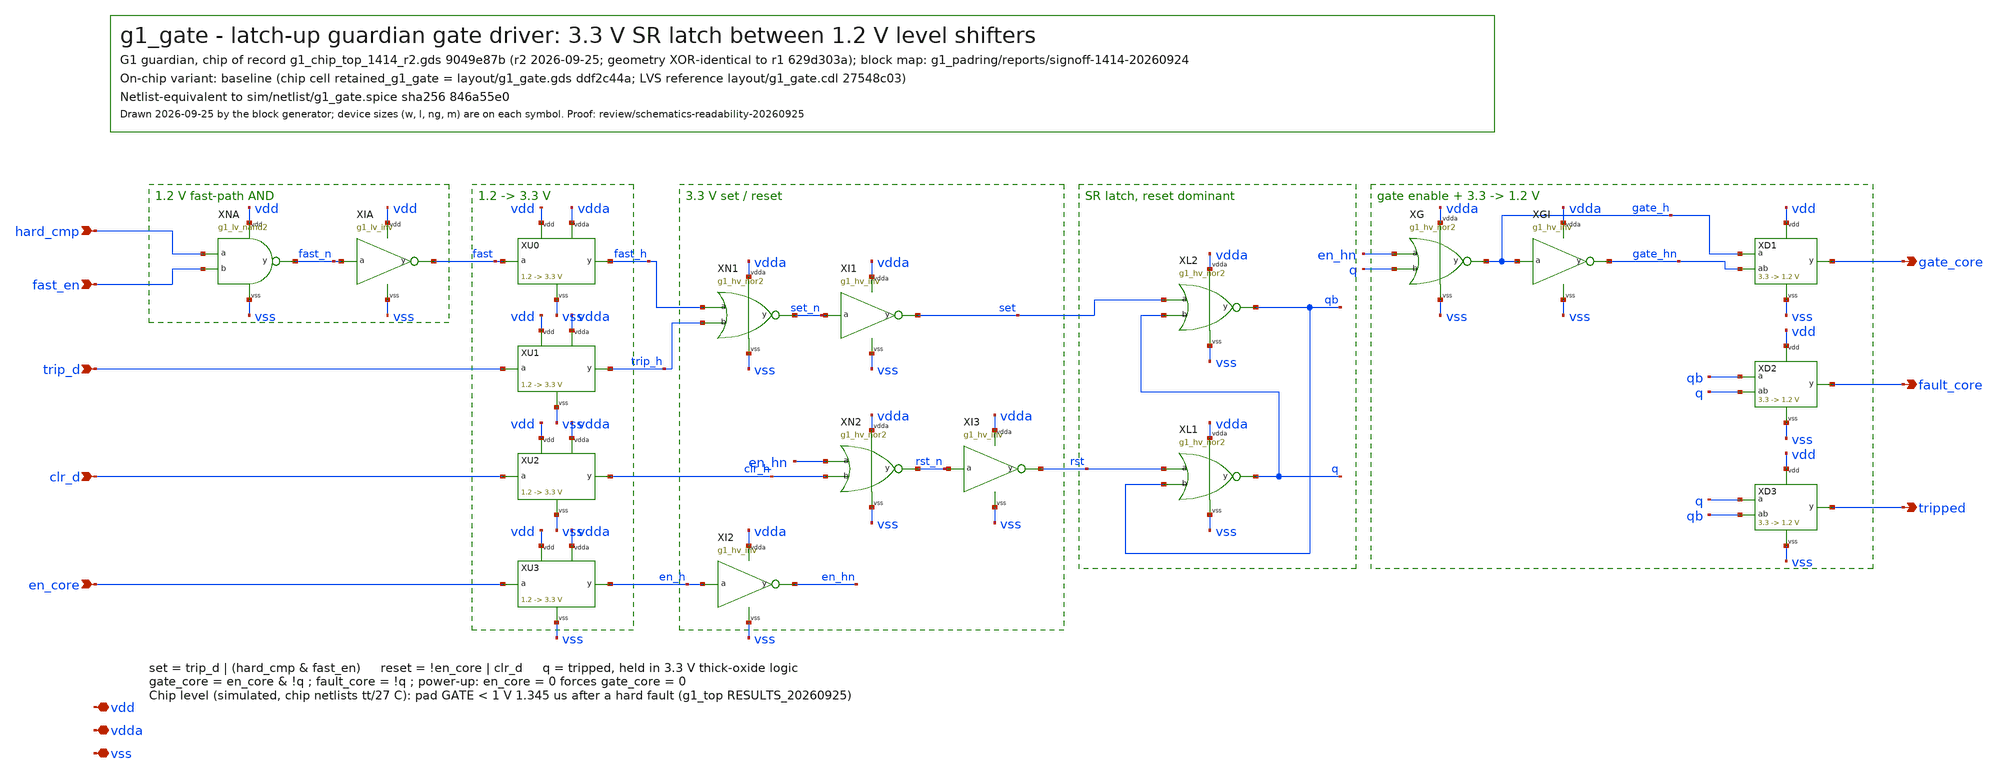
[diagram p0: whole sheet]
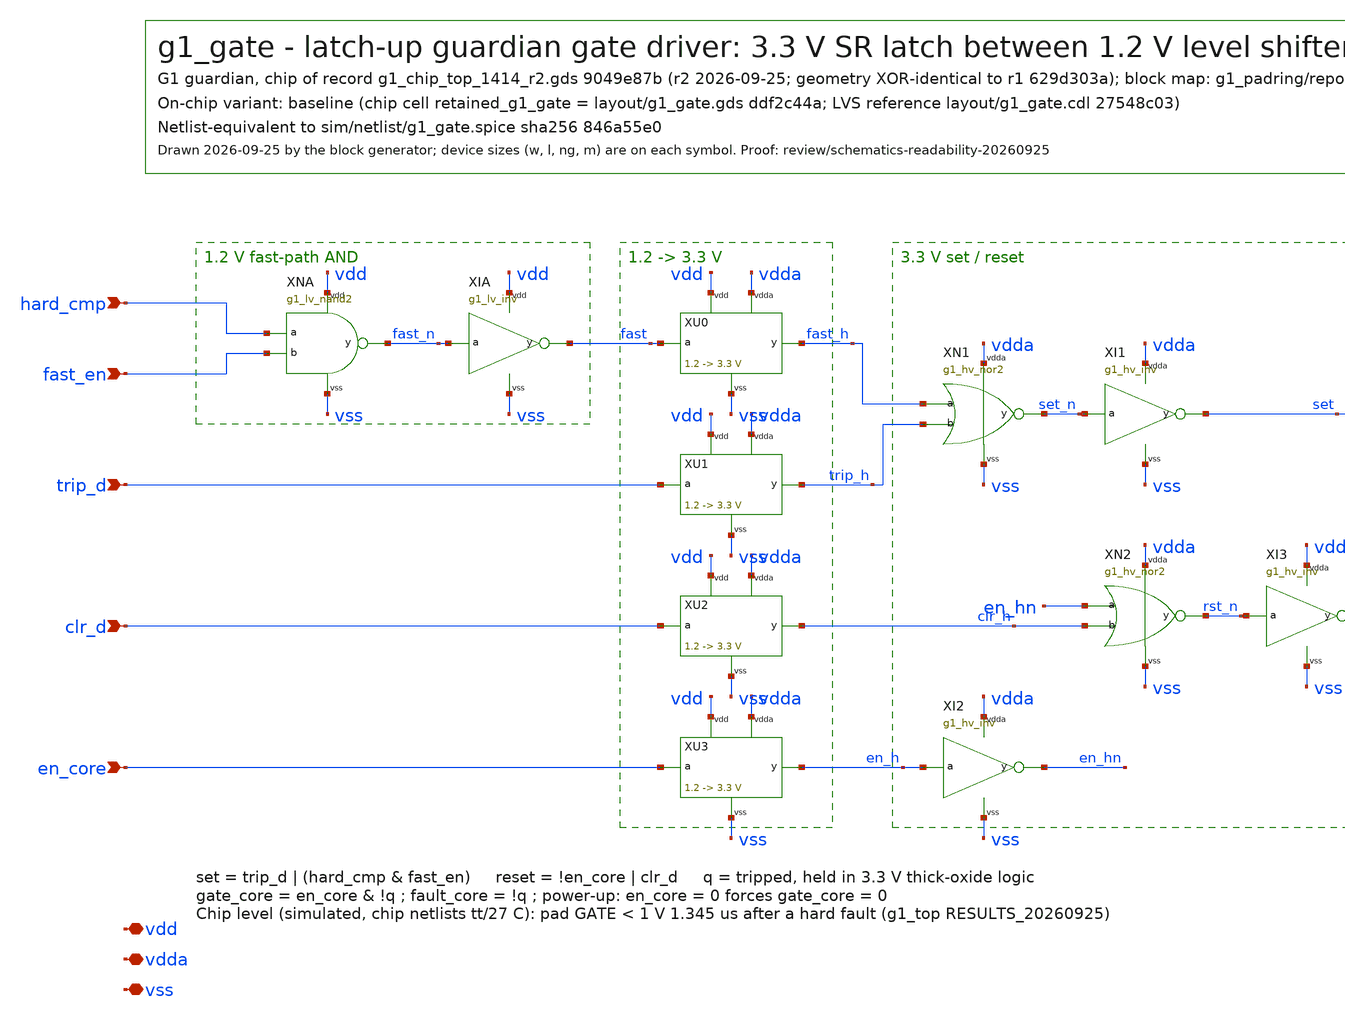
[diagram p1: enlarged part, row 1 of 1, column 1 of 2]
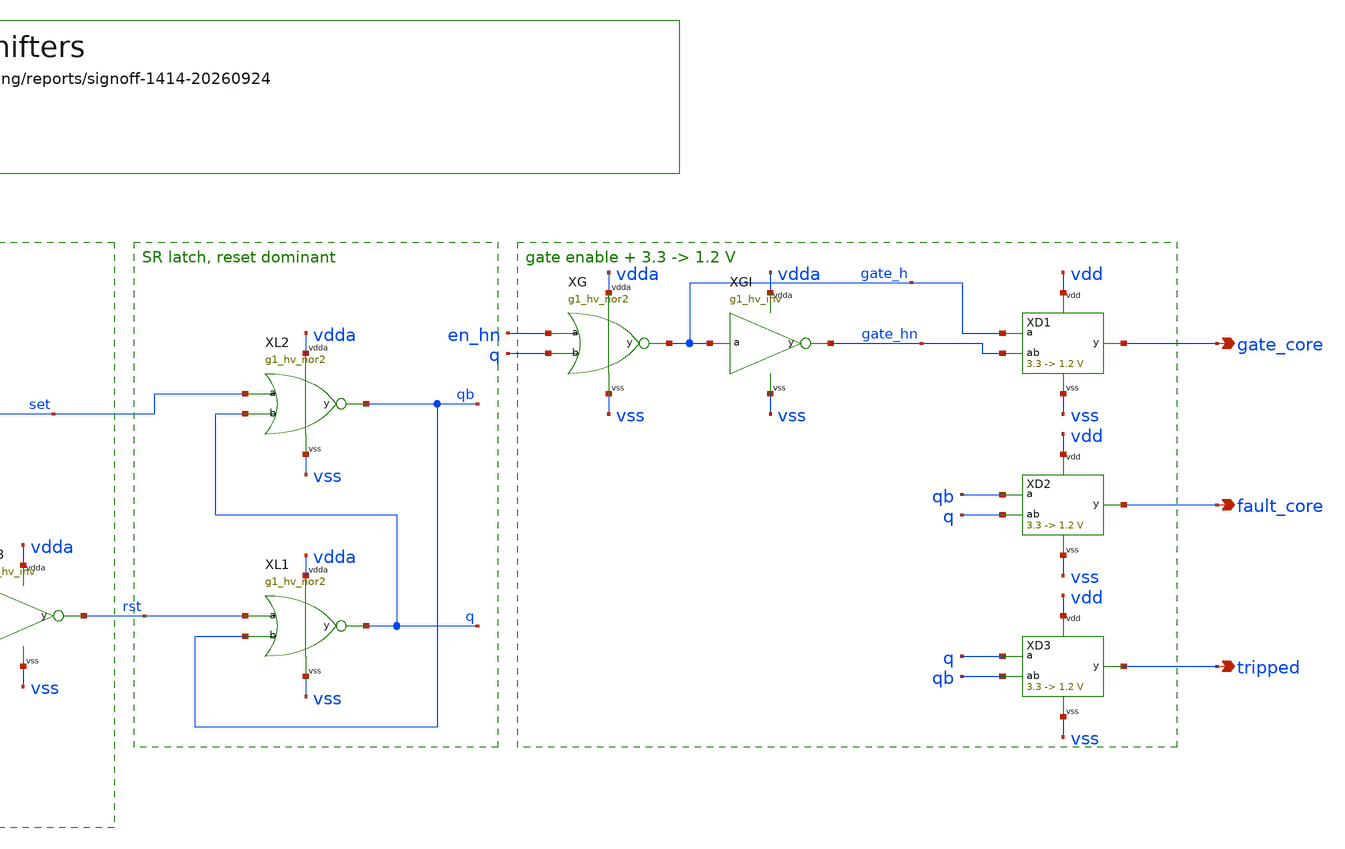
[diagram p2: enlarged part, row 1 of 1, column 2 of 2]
** sch_path: designs/g1-guardian/blocks/g1_gate/schematic/g1_gate.sch
**.subckt g1_gate trip_d clr_d fast_en hard_cmp en_core gate_core fault_core tripped vdd vdda vss
*.ipin trip_d
*.ipin clr_d
*.ipin fast_en
*.ipin hard_cmp
*.ipin en_core
*.opin gate_core
*.opin fault_core
*.opin tripped
*.iopin vdd
*.iopin vdda
*.iopin vss
XNA hard_cmp fast_en fast_n vdd vss g1_lv_nand2
XIA fast_n fast vdd vss g1_lv_inv
XU0 fast fast_h vdd vdda vss g1_lvlup
XU1 trip_d trip_h vdd vdda vss g1_lvlup
XU2 clr_d clr_h vdd vdda vss g1_lvlup
XU3 en_core en_h vdd vdda vss g1_lvlup
XN1 fast_h trip_h set_n vdda vss g1_hv_nor2
XI1 set_n set vdda vss g1_hv_inv
XI2 en_h en_hn vdda vss g1_hv_inv
XN2 en_hn clr_h rst_n vdda vss g1_hv_nor2
XI3 rst_n rst vdda vss g1_hv_inv
XL1 rst qb q vdda vss g1_hv_nor2
XL2 set q qb vdda vss g1_hv_nor2
XG en_hn q gate_h vdda vss g1_hv_nor2
XGI gate_h gate_hn vdda vss g1_hv_inv
XD1 gate_h gate_hn gate_core vdd vss g1_lvldn
XD2 qb q fault_core vdd vss g1_lvldn
XD3 q qb tripped vdd vss g1_lvldn
**.ends

* expanding   symbol:  g1_lv_nand2.sym # of pins=5
** sym_path: designs/g1-guardian/blocks/g1_gate/schematic/g1_lv_nand2.sym
** sch_path: designs/g1-guardian/blocks/g1_gate/schematic/g1_lv_nand2.sch
.subckt g1_lv_nand2 a b y vdd vss
*.ipin a
*.ipin b
*.opin y
*.iopin vdd
*.iopin vss
XMP1 y a vdd vdd sg13_lv_pmos w=2u l=0.13u ng=1 m=1 mm_ok=1
XMP2 y b vdd vdd sg13_lv_pmos w=2u l=0.13u ng=1 m=1 mm_ok=1
XMN1 y a m vss sg13_lv_nmos w=2u l=0.13u ng=1 m=1 mm_ok=1
XMN2 m b vss vss sg13_lv_nmos w=2u l=0.13u ng=1 m=1 mm_ok=1
.ends


* expanding   symbol:  g1_lv_inv.sym # of pins=4
** sym_path: designs/g1-guardian/blocks/g1_gate/schematic/g1_lv_inv.sym
** sch_path: designs/g1-guardian/blocks/g1_gate/schematic/g1_lv_inv.sch
.subckt g1_lv_inv a y vdd vss
*.ipin a
*.opin y
*.iopin vdd
*.iopin vss
XMP y a vdd vdd sg13_lv_pmos w=2u l=0.13u ng=1 m=1 mm_ok=1
XMN y a vss vss sg13_lv_nmos w=1u l=0.13u ng=1 m=1 mm_ok=1
.ends


* expanding   symbol:  g1_lvlup.sym # of pins=5
** sym_path: designs/g1-guardian/blocks/g1_gate/schematic/g1_lvlup.sym
** sch_path: designs/g1-guardian/blocks/g1_gate/schematic/g1_lvlup.sch
.subckt g1_lvlup a y vdd vdda vss
*.ipin a
*.opin y
*.iopin vdd
*.iopin vdda
*.iopin vss
XI a ab vdd vss g1_lv_inv
XMN1 nb a vss vss sg13_hv_nmos w=1.9u l=0.45u ng=1 m=1 mm_ok=1
XMN2 n ab vss vss sg13_hv_nmos w=1.9u l=0.45u ng=1 m=1 mm_ok=1
XMP1 nb n vdda vdda sg13_hv_pmos w=0.3u l=0.45u ng=1 m=1 mm_ok=1
XMP2 n nb vdda vdda sg13_hv_pmos w=0.3u l=0.45u ng=1 m=1 mm_ok=1
XO nb y vdda vss g1_hv_inv
.ends


* expanding   symbol:  g1_hv_nor2.sym # of pins=5
** sym_path: designs/g1-guardian/blocks/g1_gate/schematic/g1_hv_nor2.sym
** sch_path: designs/g1-guardian/blocks/g1_gate/schematic/g1_hv_nor2.sch
.subckt g1_hv_nor2 a b y vdda vss
*.ipin a
*.ipin b
*.opin y
*.iopin vdda
*.iopin vss
XMP1 m a vdda vdda sg13_hv_pmos w=7.8u l=0.45u ng=1 m=1 mm_ok=1
XMP2 y b m vdda sg13_hv_pmos w=7.8u l=0.45u ng=1 m=1 mm_ok=1
XMN1 y a vss vss sg13_hv_nmos w=1.9u l=0.45u ng=1 m=1 mm_ok=1
XMN2 y b vss vss sg13_hv_nmos w=1.9u l=0.45u ng=1 m=1 mm_ok=1
.ends


* expanding   symbol:  g1_hv_inv.sym # of pins=4
** sym_path: designs/g1-guardian/blocks/g1_gate/schematic/g1_hv_inv.sym
** sch_path: designs/g1-guardian/blocks/g1_gate/schematic/g1_hv_inv.sch
.subckt g1_hv_inv a y vdda vss
*.ipin a
*.opin y
*.iopin vdda
*.iopin vss
XMP y a vdda vdda sg13_hv_pmos w=3.9u l=0.45u ng=1 m=1 mm_ok=1
XMN y a vss vss sg13_hv_nmos w=1.9u l=0.45u ng=1 m=1 mm_ok=1
.ends


* expanding   symbol:  g1_lvldn.sym # of pins=5
** sym_path: designs/g1-guardian/blocks/g1_gate/schematic/g1_lvldn.sym
** sch_path: designs/g1-guardian/blocks/g1_gate/schematic/g1_lvldn.sch
.subckt g1_lvldn a ab y vdd vss
*.ipin a
*.ipin ab
*.opin y
*.iopin vdd
*.iopin vss
XMN1 yb a vss vss sg13_hv_nmos w=2u l=0.45u ng=1 m=1 mm_ok=1
XMN2 y ab vss vss sg13_hv_nmos w=2u l=0.45u ng=1 m=1 mm_ok=1
XMP1 y yb vdd vdd sg13_lv_pmos w=1u l=0.13u ng=1 m=1 mm_ok=1
XMP2 yb y vdd vdd sg13_lv_pmos w=1u l=0.13u ng=1 m=1 mm_ok=1
.ends

.end
